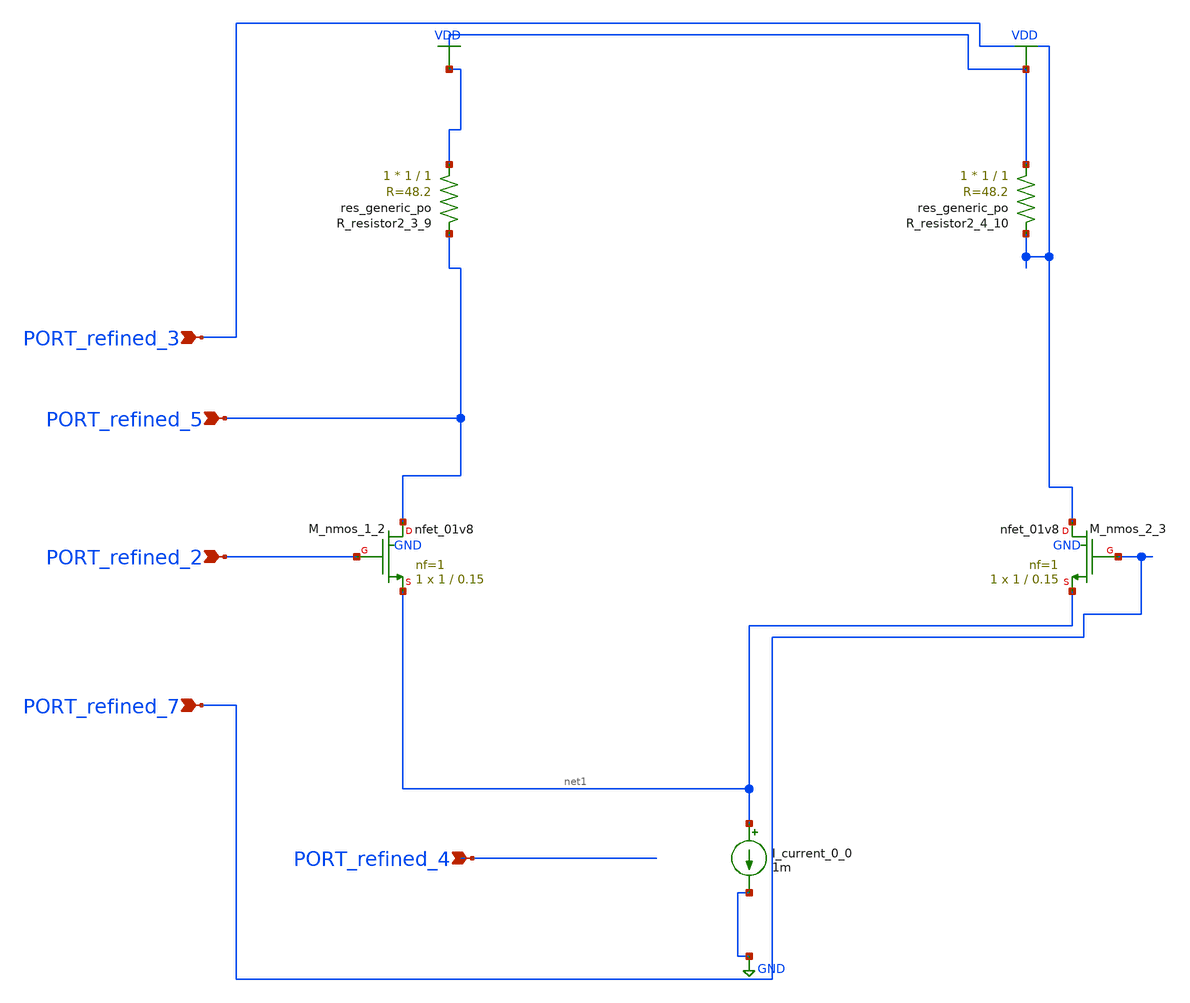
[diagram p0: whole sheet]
** sch_path: schematics/AMSNet/230.sch
**.subckt 230 PORT_refined_7 PORT_refined_2 PORT_refined_3 PORT_refined_4 PORT_refined_5
*.ipin PORT_refined_7
*.ipin PORT_refined_2
*.ipin PORT_refined_3
*.ipin PORT_refined_4
*.ipin PORT_refined_5
I_current_0_0 net1 GND 1m
XM_nmos_1_2 PORT_refined_5 PORT_refined_2 net1 GND sky130_fd_pr__nfet_01v8 L=0.15 W=1 nf=1 ad='int((1 + 1)/2) * 1 / 1 * 0.29'
+ as='int((1 + 2)/2) * 1 / 1 * 0.29' pd='2*int((1 + 1)/2) * (1 / 1 + 0.29)' ps='2*int((1 + 2)/2) * (1 / 1 + 0.29)'
+ nrd='0.29 / 1 ' nrs='0.29 / 1 ' sa=0 sb=0 sd=0 mult=1 m=1
XM_nmos_2_3 PORT_refined_3 PORT_refined_7 net1 GND sky130_fd_pr__nfet_01v8 L=0.15 W=1 nf=1 ad='int((1 + 1)/2) * 1 / 1 * 0.29'
+ as='int((1 + 2)/2) * 1 / 1 * 0.29' pd='2*int((1 + 1)/2) * (1 / 1 + 0.29)' ps='2*int((1 + 2)/2) * (1 / 1 + 0.29)'
+ nrd='0.29 / 1 ' nrs='0.29 / 1 ' sa=0 sb=0 sd=0 mult=1 m=1
XR_resistor2_3_9 VDD PORT_refined_5 sky130_fd_pr__res_generic_po W=1 L=1 m=1
XR_resistor2_4_10 VDD PORT_refined_3 sky130_fd_pr__res_generic_po W=1 L=1 m=1
**.ends
.GLOBAL GND
.GLOBAL VDD
.end
